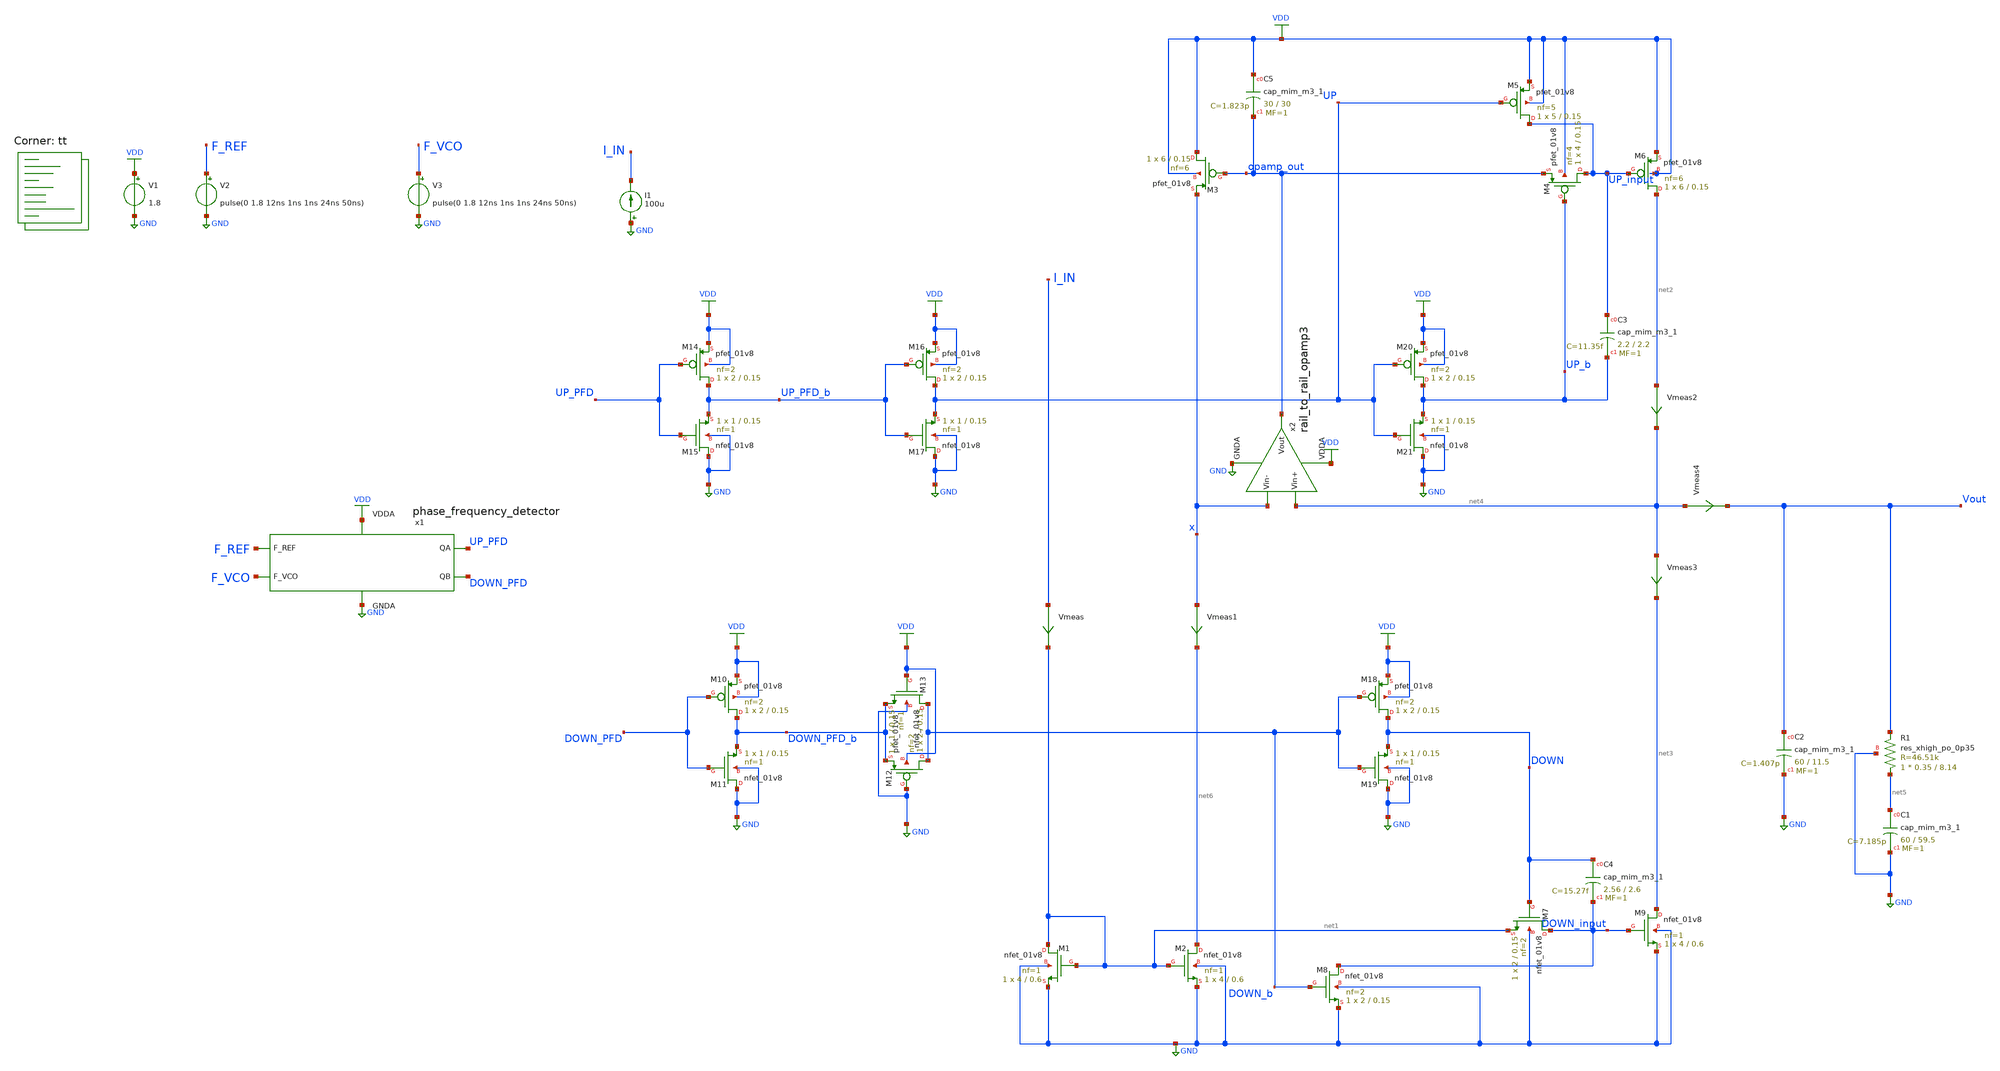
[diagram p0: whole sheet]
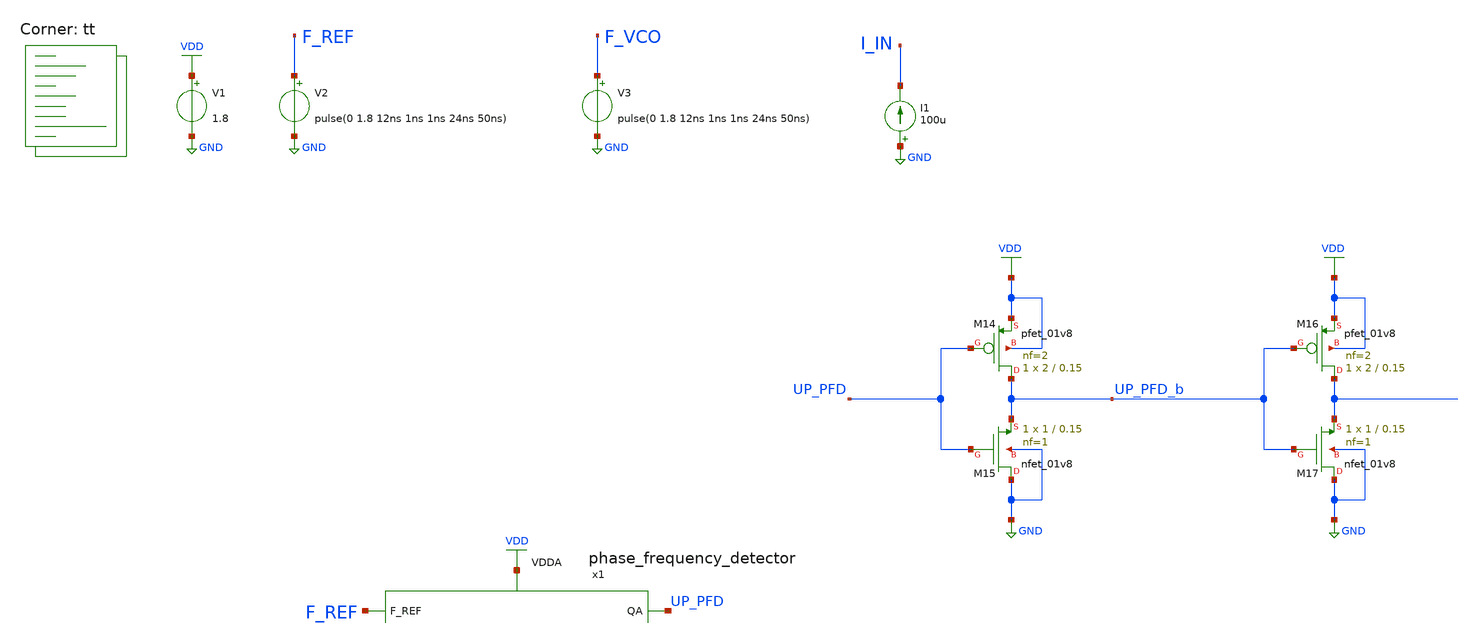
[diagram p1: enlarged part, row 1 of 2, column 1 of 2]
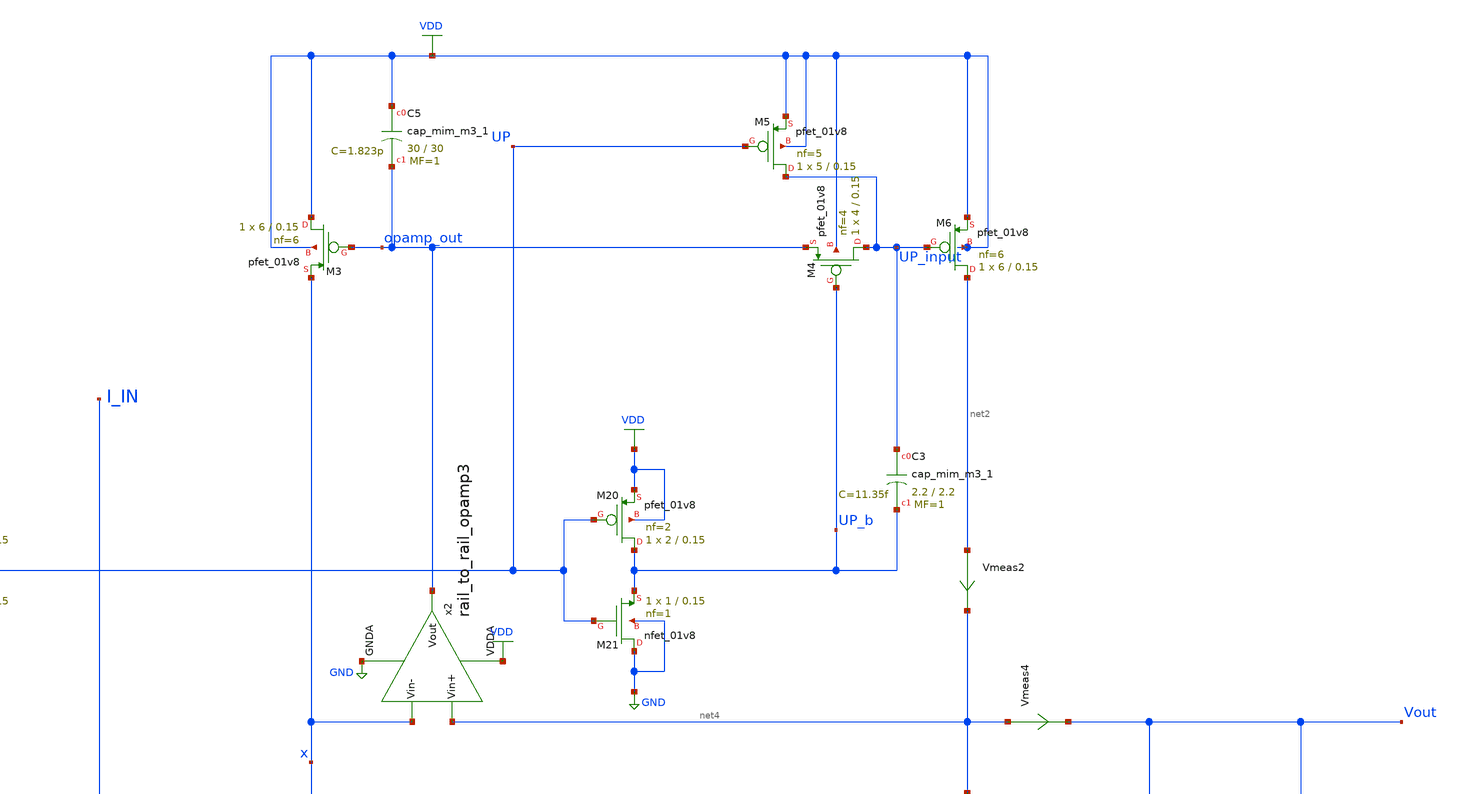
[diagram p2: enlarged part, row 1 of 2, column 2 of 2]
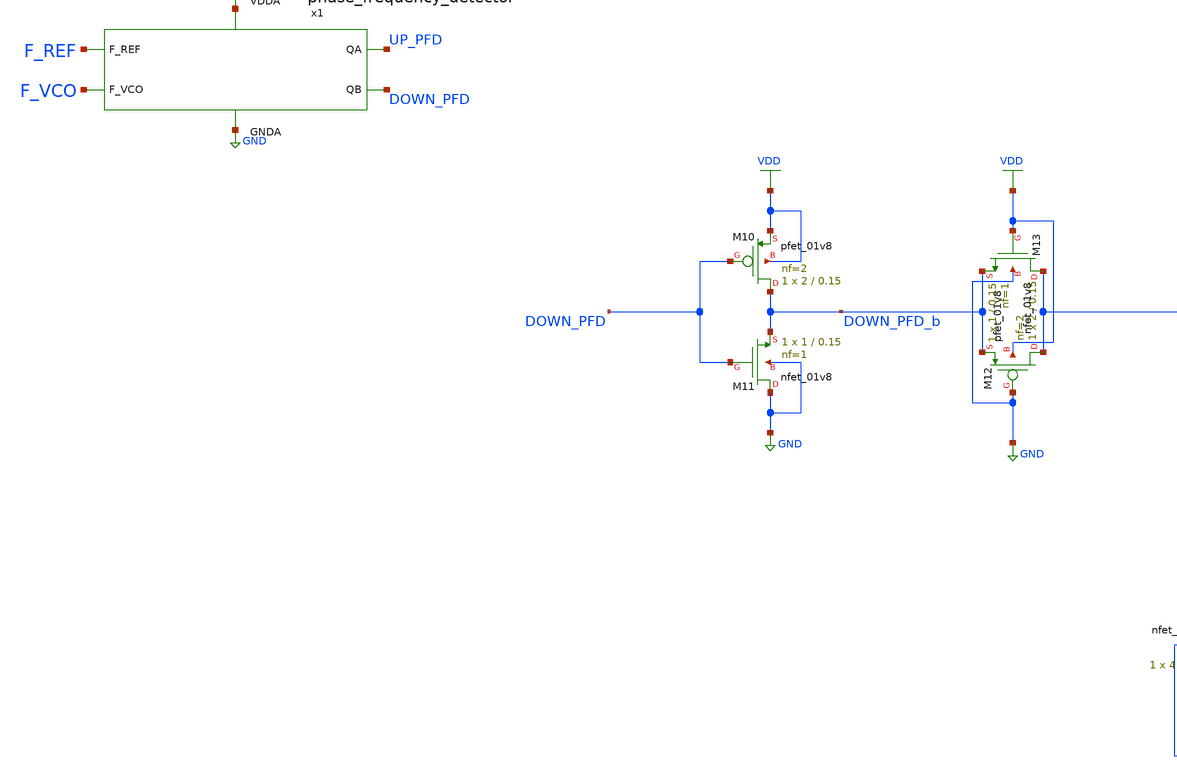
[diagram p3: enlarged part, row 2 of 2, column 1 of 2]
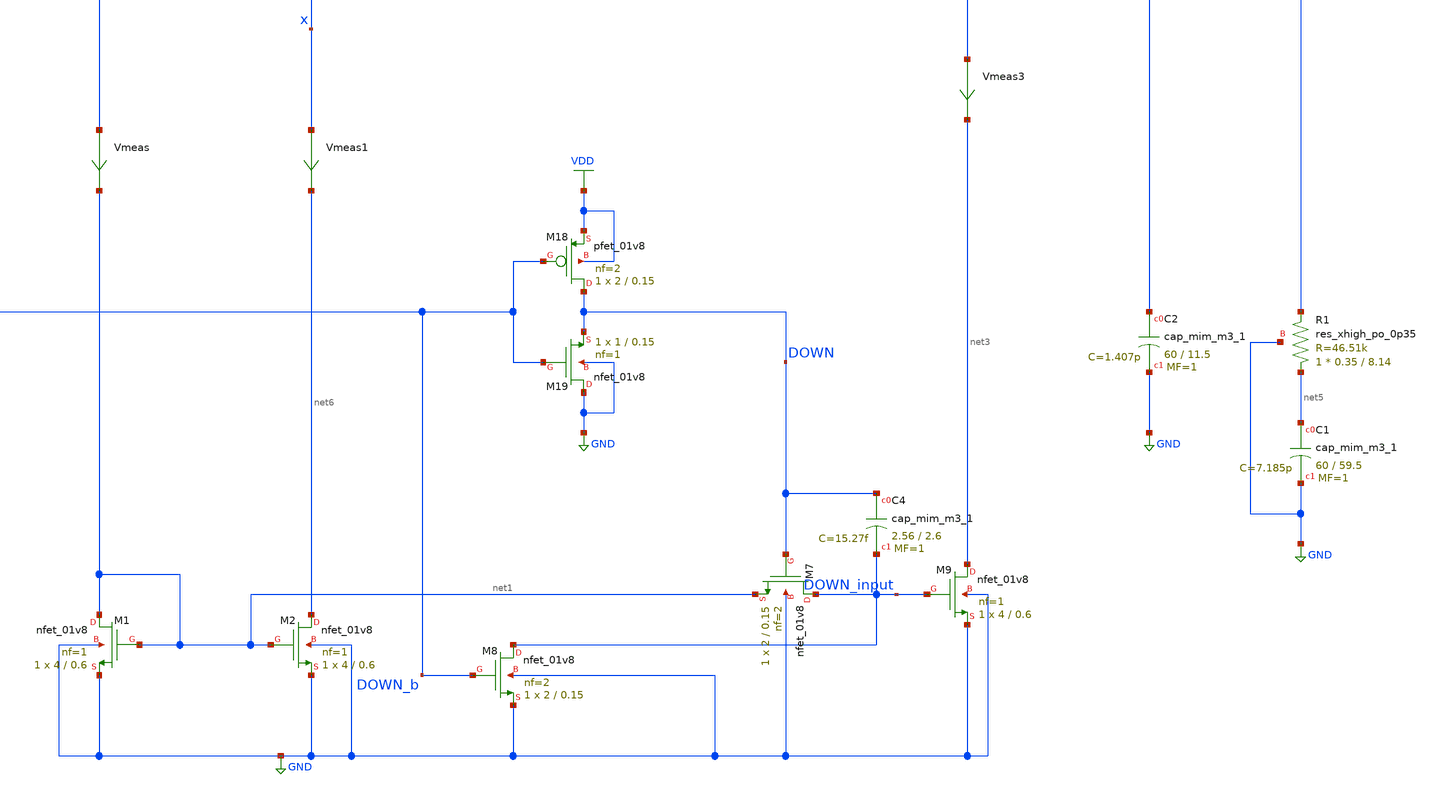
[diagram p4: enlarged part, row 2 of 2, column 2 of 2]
** sch_path: projects/pll/charge_pump/xschem_ngspice/pfd_charge_pump_dead_zone_check_4.sch
**.subckt pfd_charge_pump_dead_zone_check_4
V1 VDD GND 1.8
V2 F_REF GND pulse(0 1.8 12ns 1ns 1ns 24ns 50ns)
V3 F_VCO GND pulse(0 1.8 12ns 1ns 1ns 24ns 50ns)
x1 F_REF F_VCO VDD UP_PFD DOWN_PFD GND phase_frequency_detector
I1 GND I_IN 100u
XM1 net1 net1 GND GND sky130_fd_pr__nfet_01v8 L=0.6 W=4 nf=1 ad='int((nf+1)/2) * W/nf * 0.29' as='int((nf+2)/2) * W/nf * 0.29'
+ pd='2*int((nf+1)/2) * (W/nf + 0.29)' ps='2*int((nf+2)/2) * (W/nf + 0.29)' nrd='0.29 / W' nrs='0.29 / W'
+ sa=0 sb=0 sd=0 mult=1 m=1
XM2 net6 net1 GND GND sky130_fd_pr__nfet_01v8 L=0.6 W=4 nf=1 ad='int((nf+1)/2) * W/nf * 0.29' as='int((nf+2)/2) * W/nf * 0.29'
+ pd='2*int((nf+1)/2) * (W/nf + 0.29)' ps='2*int((nf+2)/2) * (W/nf + 0.29)' nrd='0.29 / W' nrs='0.29 / W'
+ sa=0 sb=0 sd=0 mult=1 m=1
XM3 VDD opamp_out x VDD sky130_fd_pr__pfet_01v8 L=0.15 W=6 nf=6 ad='int((nf+1)/2) * W/nf * 0.29' as='int((nf+2)/2) * W/nf * 0.29'
+ pd='2*int((nf+1)/2) * (W/nf + 0.29)' ps='2*int((nf+2)/2) * (W/nf + 0.29)' nrd='0.29 / W' nrs='0.29 / W'
+ sa=0 sb=0 sd=0 mult=1 m=1
XM4 UP_input UP_b opamp_out VDD sky130_fd_pr__pfet_01v8 L=0.15 W=4 nf=4 ad='int((nf+1)/2) * W/nf * 0.29'
+ as='int((nf+2)/2) * W/nf * 0.29' pd='2*int((nf+1)/2) * (W/nf + 0.29)' ps='2*int((nf+2)/2) * (W/nf + 0.29)'
+ nrd='0.29 / W' nrs='0.29 / W' sa=0 sb=0 sd=0 mult=1 m=1
XM5 UP_input UP VDD VDD sky130_fd_pr__pfet_01v8 L=0.15 W=5 nf=5 ad='int((nf+1)/2) * W/nf * 0.29' as='int((nf+2)/2) * W/nf * 0.29'
+ pd='2*int((nf+1)/2) * (W/nf + 0.29)' ps='2*int((nf+2)/2) * (W/nf + 0.29)' nrd='0.29 / W' nrs='0.29 / W'
+ sa=0 sb=0 sd=0 mult=1 m=1
XM6 net2 UP_input VDD VDD sky130_fd_pr__pfet_01v8 L=0.15 W=6 nf=6 ad='int((nf+1)/2) * W/nf * 0.29' as='int((nf+2)/2) * W/nf * 0.29'
+ pd='2*int((nf+1)/2) * (W/nf + 0.29)' ps='2*int((nf+2)/2) * (W/nf + 0.29)' nrd='0.29 / W' nrs='0.29 / W'
+ sa=0 sb=0 sd=0 mult=1 m=1
XM7 DOWN_input DOWN net1 GND sky130_fd_pr__nfet_01v8 L=0.15 W=2 nf=2 ad='int((nf+1)/2) * W/nf * 0.29'
+ as='int((nf+2)/2) * W/nf * 0.29' pd='2*int((nf+1)/2) * (W/nf + 0.29)' ps='2*int((nf+2)/2) * (W/nf + 0.29)'
+ nrd='0.29 / W' nrs='0.29 / W' sa=0 sb=0 sd=0 mult=1 m=1
XM8 DOWN_input DOWN_b GND GND sky130_fd_pr__nfet_01v8 L=0.15 W=2 nf=2 ad='int((nf+1)/2) * W/nf * 0.29'
+ as='int((nf+2)/2) * W/nf * 0.29' pd='2*int((nf+1)/2) * (W/nf + 0.29)' ps='2*int((nf+2)/2) * (W/nf + 0.29)'
+ nrd='0.29 / W' nrs='0.29 / W' sa=0 sb=0 sd=0 mult=1 m=1
XM9 net3 DOWN_input GND GND sky130_fd_pr__nfet_01v8 L=0.6 W=4 nf=1 ad='int((nf+1)/2) * W/nf * 0.29' as='int((nf+2)/2) * W/nf * 0.29'
+ pd='2*int((nf+1)/2) * (W/nf + 0.29)' ps='2*int((nf+2)/2) * (W/nf + 0.29)' nrd='0.29 / W' nrs='0.29 / W'
+ sa=0 sb=0 sd=0 mult=1 m=1
XC2 Vout GND sky130_fd_pr__cap_mim_m3_1 W=60 L=11.5 MF=1 m=1
XC1 net5 GND sky130_fd_pr__cap_mim_m3_1 W=60 L=59.5 MF=1 m=1
x2 VDD net4 x opamp_out GND rail_to_rail_opamp3
XR1 net5 Vout GND sky130_fd_pr__res_xhigh_po_0p35 L=8.14 mult=1 m=1
XM12 DOWN_b GND DOWN_PFD_b VDD sky130_fd_pr__pfet_01v8 L=0.15 W=2 nf=2 ad='int((nf+1)/2) * W/nf * 0.29'
+ as='int((nf+2)/2) * W/nf * 0.29' pd='2*int((nf+1)/2) * (W/nf + 0.29)' ps='2*int((nf+2)/2) * (W/nf + 0.29)'
+ nrd='0.29 / W' nrs='0.29 / W' sa=0 sb=0 sd=0 mult=1 m=1
XM13 DOWN_b VDD DOWN_PFD_b GND sky130_fd_pr__nfet_01v8 L=0.15 W=1 nf=1 ad='int((nf+1)/2) * W/nf * 0.29'
+ as='int((nf+2)/2) * W/nf * 0.29' pd='2*int((nf+1)/2) * (W/nf + 0.29)' ps='2*int((nf+2)/2) * (W/nf + 0.29)'
+ nrd='0.29 / W' nrs='0.29 / W' sa=0 sb=0 sd=0 mult=1 m=1
XC5 VDD opamp_out sky130_fd_pr__cap_mim_m3_1 W=30 L=30 MF=1 m=1
XM10 DOWN_PFD_b DOWN_PFD VDD VDD sky130_fd_pr__pfet_01v8 L=0.15 W=2 nf=2 ad='int((nf+1)/2) * W/nf * 0.29'
+ as='int((nf+2)/2) * W/nf * 0.29' pd='2*int((nf+1)/2) * (W/nf + 0.29)' ps='2*int((nf+2)/2) * (W/nf + 0.29)'
+ nrd='0.29 / W' nrs='0.29 / W' sa=0 sb=0 sd=0 mult=1 m=1
XM11 GND DOWN_PFD DOWN_PFD_b GND sky130_fd_pr__nfet_01v8 L=0.15 W=1 nf=1 ad='int((nf+1)/2) * W/nf * 0.29'
+ as='int((nf+2)/2) * W/nf * 0.29' pd='2*int((nf+1)/2) * (W/nf + 0.29)' ps='2*int((nf+2)/2) * (W/nf + 0.29)'
+ nrd='0.29 / W' nrs='0.29 / W' sa=0 sb=0 sd=0 mult=1 m=1
XM14 UP_PFD_b UP_PFD VDD VDD sky130_fd_pr__pfet_01v8 L=0.15 W=2 nf=2 ad='int((nf+1)/2) * W/nf * 0.29'
+ as='int((nf+2)/2) * W/nf * 0.29' pd='2*int((nf+1)/2) * (W/nf + 0.29)' ps='2*int((nf+2)/2) * (W/nf + 0.29)'
+ nrd='0.29 / W' nrs='0.29 / W' sa=0 sb=0 sd=0 mult=1 m=1
XM15 GND UP_PFD UP_PFD_b GND sky130_fd_pr__nfet_01v8 L=0.15 W=1 nf=1 ad='int((nf+1)/2) * W/nf * 0.29'
+ as='int((nf+2)/2) * W/nf * 0.29' pd='2*int((nf+1)/2) * (W/nf + 0.29)' ps='2*int((nf+2)/2) * (W/nf + 0.29)'
+ nrd='0.29 / W' nrs='0.29 / W' sa=0 sb=0 sd=0 mult=1 m=1
XM16 UP UP_PFD_b VDD VDD sky130_fd_pr__pfet_01v8 L=0.15 W=2 nf=2 ad='int((nf+1)/2) * W/nf * 0.29' as='int((nf+2)/2) * W/nf * 0.29'
+ pd='2*int((nf+1)/2) * (W/nf + 0.29)' ps='2*int((nf+2)/2) * (W/nf + 0.29)' nrd='0.29 / W' nrs='0.29 / W'
+ sa=0 sb=0 sd=0 mult=1 m=1
XM17 GND UP_PFD_b UP GND sky130_fd_pr__nfet_01v8 L=0.15 W=1 nf=1 ad='int((nf+1)/2) * W/nf * 0.29' as='int((nf+2)/2) * W/nf * 0.29'
+ pd='2*int((nf+1)/2) * (W/nf + 0.29)' ps='2*int((nf+2)/2) * (W/nf + 0.29)' nrd='0.29 / W' nrs='0.29 / W'
+ sa=0 sb=0 sd=0 mult=1 m=1
XM18 DOWN DOWN_b VDD VDD sky130_fd_pr__pfet_01v8 L=0.15 W=2 nf=2 ad='int((nf+1)/2) * W/nf * 0.29' as='int((nf+2)/2) * W/nf * 0.29'
+ pd='2*int((nf+1)/2) * (W/nf + 0.29)' ps='2*int((nf+2)/2) * (W/nf + 0.29)' nrd='0.29 / W' nrs='0.29 / W'
+ sa=0 sb=0 sd=0 mult=1 m=1
XM19 GND DOWN_b DOWN GND sky130_fd_pr__nfet_01v8 L=0.15 W=1 nf=1 ad='int((nf+1)/2) * W/nf * 0.29' as='int((nf+2)/2) * W/nf * 0.29'
+ pd='2*int((nf+1)/2) * (W/nf + 0.29)' ps='2*int((nf+2)/2) * (W/nf + 0.29)' nrd='0.29 / W' nrs='0.29 / W'
+ sa=0 sb=0 sd=0 mult=1 m=1
XM20 UP_b UP VDD VDD sky130_fd_pr__pfet_01v8 L=0.15 W=2 nf=2 ad='int((nf+1)/2) * W/nf * 0.29' as='int((nf+2)/2) * W/nf * 0.29'
+ pd='2*int((nf+1)/2) * (W/nf + 0.29)' ps='2*int((nf+2)/2) * (W/nf + 0.29)' nrd='0.29 / W' nrs='0.29 / W'
+ sa=0 sb=0 sd=0 mult=1 m=1
XM21 GND UP UP_b GND sky130_fd_pr__nfet_01v8 L=0.15 W=1 nf=1 ad='int((nf+1)/2) * W/nf * 0.29' as='int((nf+2)/2) * W/nf * 0.29'
+ pd='2*int((nf+1)/2) * (W/nf + 0.29)' ps='2*int((nf+2)/2) * (W/nf + 0.29)' nrd='0.29 / W' nrs='0.29 / W'
+ sa=0 sb=0 sd=0 mult=1 m=1
Vmeas I_IN net1 0
.save i(vmeas)
XC3 UP_input UP_b sky130_fd_pr__cap_mim_m3_1 W=2.2 L=2.2 MF=1 m=1
XC4 DOWN DOWN_input sky130_fd_pr__cap_mim_m3_1 W=2.56 L=2.6 MF=1 m=1
Vmeas1 x net6 0
.save i(vmeas1)
Vmeas2 net2 net4 0
.save i(vmeas2)
Vmeas3 net4 net3 0
.save i(vmeas3)
Vmeas4 net4 Vout 0
.save i(vmeas4)
**** begin user architecture code
.lib $::SKYWATER_MODELS/sky130.lib.spice tt



.include /foss/pdks/sky130A/libs.ref/sky130_fd_sc_hd/spice/sky130_fd_sc_hd.spice

.option method=gear
.option wnflag=1

.ic v(vout) = 0.9

.control
  let start_delay = 0ns
  let stop_delay = 24ns
  let index = -12
  dowhile start_delay <= stop_delay

    alter @V3[pulse] = [ 0 1.8 $&start_delay 1ns 1ns 24ns 50ns ]
    save i(vmeas2#branch) i(vmeas3#branch) i(vmeas4#branch) v(F_REF) v(F_VCO) v(vout)
    tran 5ps 1us
    remzerovec
    linearize i(vmeas2) i(vmeas3) i(vmeas4) v(F_REF) v(F_VCO) v(vout)
    echo $&start_delay
    write pfd_charge_pump_dead_zone_check_4_{$&index}.raw
    wrdata /foss/designs/my_design/projects/pll/charge_pump/xschem_ngspice/pfd_charge_pump_dead_zone_check_4_{$&index}.txt
+ i(vmeas4)
    set appendwrite
    reset
    let index = index + 1
    let start_delay = start_delay + 1ns

  end
.endc



**** end user architecture code
**.ends
.GLOBAL GND
.GLOBAL VDD
.end
